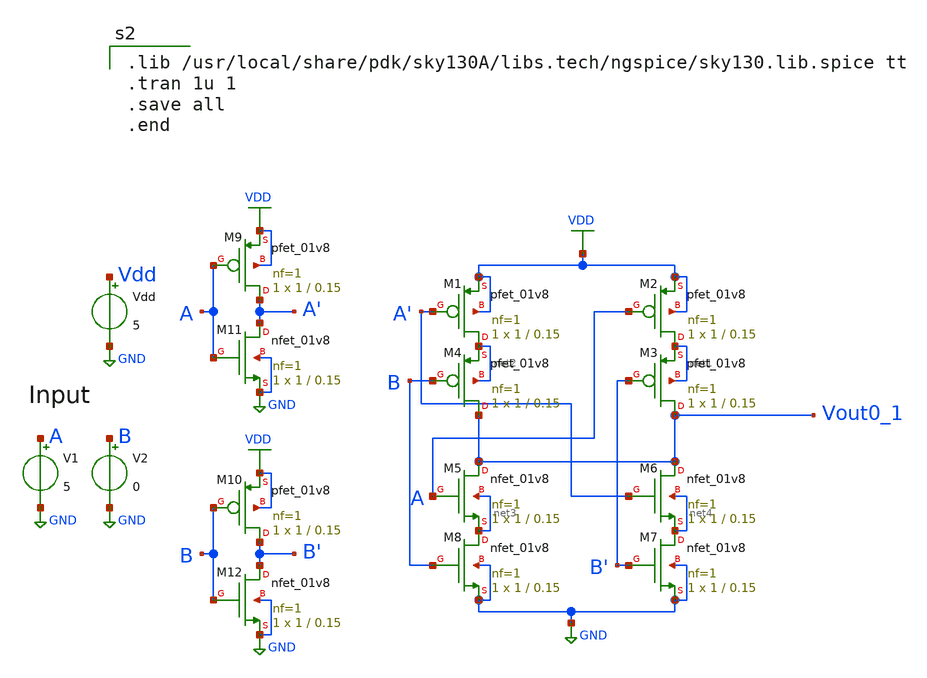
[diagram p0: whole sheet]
** sch_path: XOR.sch
**.subckt XOR
XM1 net2 A' VDD VDD sky130_fd_pr__pfet_01v8 L=0.15 W=1 nf=1 ad='int((1 + 1)/2) * 1 / 1 * 0.29' as='int((1
+ + 2)/2) * 1 / 1 * 0.29' pd='2*int((1 + 1)/2) * (1 / 1 + 0.29)' ps='2*int((1 + 2)/2) * (1 / 1 + 0.29)' nrd='0.29
+ / 1 ' nrs='0.29 / 1 ' sa=0 sb=0 sd=0 mult=1 m=1
XM2 net1 A VDD VDD sky130_fd_pr__pfet_01v8 L=0.15 W=1 nf=1 ad='int((1 + 1)/2) * 1 / 1 * 0.29' as='int((1
+ + 2)/2) * 1 / 1 * 0.29' pd='2*int((1 + 1)/2) * (1 / 1 + 0.29)' ps='2*int((1 + 2)/2) * (1 / 1 + 0.29)' nrd='0.29
+ / 1 ' nrs='0.29 / 1 ' sa=0 sb=0 sd=0 mult=1 m=1
XM3 Vout0_1 B' net1 net1 sky130_fd_pr__pfet_01v8 L=0.15 W=1 nf=1 ad='int((1 + 1)/2) * 1 / 1 * 0.29' as='int((1 + 2)/2) * 1 / 1 * 0.29'
+ pd='2*int((1 + 1)/2) * (1 / 1 + 0.29)' ps='2*int((1 + 2)/2) * (1 / 1 + 0.29)' nrd='0.29 / 1 ' nrs='0.29 / 1 '
+ sa=0 sb=0 sd=0 mult=1 m=1
XM4 Vout0_1 B net2 net2 sky130_fd_pr__pfet_01v8 L=0.15 W=1 nf=1 ad='int((1 + 1)/2) * 1 / 1 * 0.29' as='int((1 + 2)/2) * 1 / 1 * 0.29'
+ pd='2*int((1 + 1)/2) * (1 / 1 + 0.29)' ps='2*int((1 + 2)/2) * (1 / 1 + 0.29)' nrd='0.29 / 1 ' nrs='0.29 / 1 '
+ sa=0 sb=0 sd=0 mult=1 m=1
XM5 Vout0_1 A net3 net3 sky130_fd_pr__nfet_01v8 L=0.15 W=1 nf=1 ad='int((1 + 1)/2) * 1 / 1 * 0.29' as='int((1 + 2)/2) * 1 / 1 * 0.29'
+ pd='2*int((1 + 1)/2) * (1 / 1 + 0.29)' ps='2*int((1 + 2)/2) * (1 / 1 + 0.29)' nrd='0.29 / 1 ' nrs='0.29 / 1 '
+ sa=0 sb=0 sd=0 mult=1 m=1
XM6 Vout0_1 A' net4 net4 sky130_fd_pr__nfet_01v8 L=0.15 W=1 nf=1 ad='int((1 + 1)/2) * 1 / 1 * 0.29' as='int((1
+ + 2)/2) * 1 / 1 * 0.29' pd='2*int((1 + 1)/2) * (1 / 1 + 0.29)' ps='2*int((1 + 2)/2) * (1 / 1 + 0.29)' nrd='0.29
+ / 1 ' nrs='0.29 / 1 ' sa=0 sb=0 sd=0 mult=1 m=1
XM7 net4 B' GND GND sky130_fd_pr__nfet_01v8 L=0.15 W=1 nf=1 ad='int((1 + 1)/2) * 1 / 1 * 0.29' as='int((1 + 2)/2) * 1 / 1 * 0.29'
+ pd='2*int((1 + 1)/2) * (1 / 1 + 0.29)' ps='2*int((1 + 2)/2) * (1 / 1 + 0.29)' nrd='0.29 / 1 ' nrs='0.29 / 1 '
+ sa=0 sb=0 sd=0 mult=1 m=1
XM8 net3 B GND GND sky130_fd_pr__nfet_01v8 L=0.15 W=1 nf=1 ad='int((1 + 1)/2) * 1 / 1 * 0.29' as='int((1 + 2)/2) * 1 / 1 * 0.29'
+ pd='2*int((1 + 1)/2) * (1 / 1 + 0.29)' ps='2*int((1 + 2)/2) * (1 / 1 + 0.29)' nrd='0.29 / 1 ' nrs='0.29 / 1 '
+ sa=0 sb=0 sd=0 mult=1 m=1
Vdd Vdd GND 5
XM9 A' A VDD VDD sky130_fd_pr__pfet_01v8 L=0.15 W=1 nf=1 ad='int((1 + 1)/2) * 1 / 1 * 0.29' as='int((1
+ + 2)/2) * 1 / 1 * 0.29' pd='2*int((1 + 1)/2) * (1 / 1 + 0.29)' ps='2*int((1 + 2)/2) * (1 / 1 + 0.29)' nrd='0.29
+ / 1 ' nrs='0.29 / 1 ' sa=0 sb=0 sd=0 mult=1 m=1
XM11 A' A GND GND sky130_fd_pr__nfet_01v8 L=0.15 W=1 nf=1 ad='int((1 + 1)/2) * 1 / 1 * 0.29' as='int((1 + 2)/2) * 1 / 1 * 0.29'
+ pd='2*int((1 + 1)/2) * (1 / 1 + 0.29)' ps='2*int((1 + 2)/2) * (1 / 1 + 0.29)' nrd='0.29 / 1 ' nrs='0.29 / 1 '
+ sa=0 sb=0 sd=0 mult=1 m=1
V1 A GND 5
V2 B GND 0
XM10 B' B VDD VDD sky130_fd_pr__pfet_01v8 L=0.15 W=1 nf=1 ad='int((1 + 1)/2) * 1 / 1 * 0.29' as='int((1
+ + 2)/2) * 1 / 1 * 0.29' pd='2*int((1 + 1)/2) * (1 / 1 + 0.29)' ps='2*int((1 + 2)/2) * (1 / 1 + 0.29)' nrd='0.29
+ / 1 ' nrs='0.29 / 1 ' sa=0 sb=0 sd=0 mult=1 m=1
XM12 B' B GND GND sky130_fd_pr__nfet_01v8 L=0.15 W=1 nf=1 ad='int((1 + 1)/2) * 1 / 1 * 0.29' as='int((1 + 2)/2) * 1 / 1 * 0.29'
+ pd='2*int((1 + 1)/2) * (1 / 1 + 0.29)' ps='2*int((1 + 2)/2) * (1 / 1 + 0.29)' nrd='0.29 / 1 ' nrs='0.29 / 1 '
+ sa=0 sb=0 sd=0 mult=1 m=1
**** begin user architecture code

.lib /usr/local/share/pdk/sky130A/libs.tech/ngspice/sky130.lib.spice tt
.tran 1u 1
.save all
.end

**** end user architecture code
**.ends
.GLOBAL VDD
.GLOBAL GND
.end
